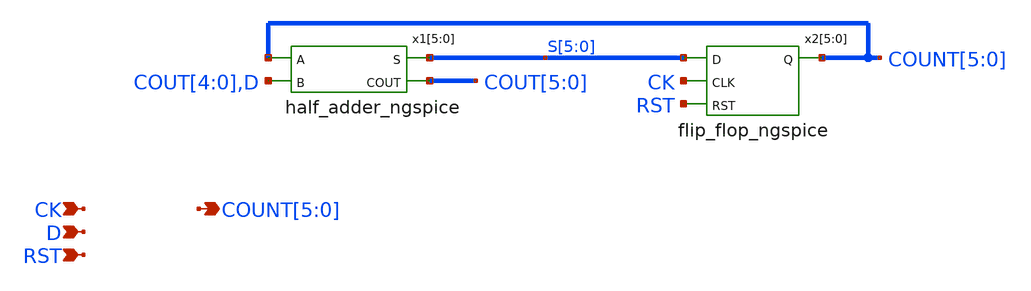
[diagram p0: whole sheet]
** sch_path: xschem_libs_newsym/ngspice/counter_6bit_ngspice/schematic/counter_6bit_ngspice.sch
* Copyright (C) 1998-2024 Stefan Frederik Schippers
* This program is free software; you can redistribute it and/or modify
* it under the terms of the GNU General Public License as published by
* the Free Software Foundation; either version 2 of the License, or
* (at your option) any later version.
* This program is distributed in the hope that it will be useful,
* but WITHOUT ANY WARRANTY; without even the implied warranty of
* MERCHANTABILITY or FITNESS FOR A PARTICULAR PURPOSE.  See the
* GNU General Public License for more details.
* You should have received a copy of the GNU General Public License
* along with this program; if not, write to the Free Software
**.subckt counter_6bit_ngspice RST D COUNT[5],COUNT[4],COUNT[3],COUNT[2],COUNT[1],COUNT[0] CK
*.ipin RST
*.ipin D
*.opin COUNT[5],COUNT[4],COUNT[3],COUNT[2],COUNT[1],COUNT[0]
*.ipin CK
x2[5] S[5] CK COUNT[5] RST flip_flop_ngspice
x2[4] S[4] CK COUNT[4] RST flip_flop_ngspice
x2[3] S[3] CK COUNT[3] RST flip_flop_ngspice
x2[2] S[2] CK COUNT[2] RST flip_flop_ngspice
x2[1] S[1] CK COUNT[1] RST flip_flop_ngspice
x2[0] S[0] CK COUNT[0] RST flip_flop_ngspice
x1[5] COUNT[5] S[5] COUT[5] COUT[4] half_adder_ngspice
x1[4] COUNT[4] S[4] COUT[4] COUT[3] half_adder_ngspice
x1[3] COUNT[3] S[3] COUT[3] COUT[2] half_adder_ngspice
x1[2] COUNT[2] S[2] COUT[2] COUT[1] half_adder_ngspice
x1[1] COUNT[1] S[1] COUT[1] COUT[0] half_adder_ngspice
x1[0] COUNT[0] S[0] COUT[0] D half_adder_ngspice
**.ends
.end
